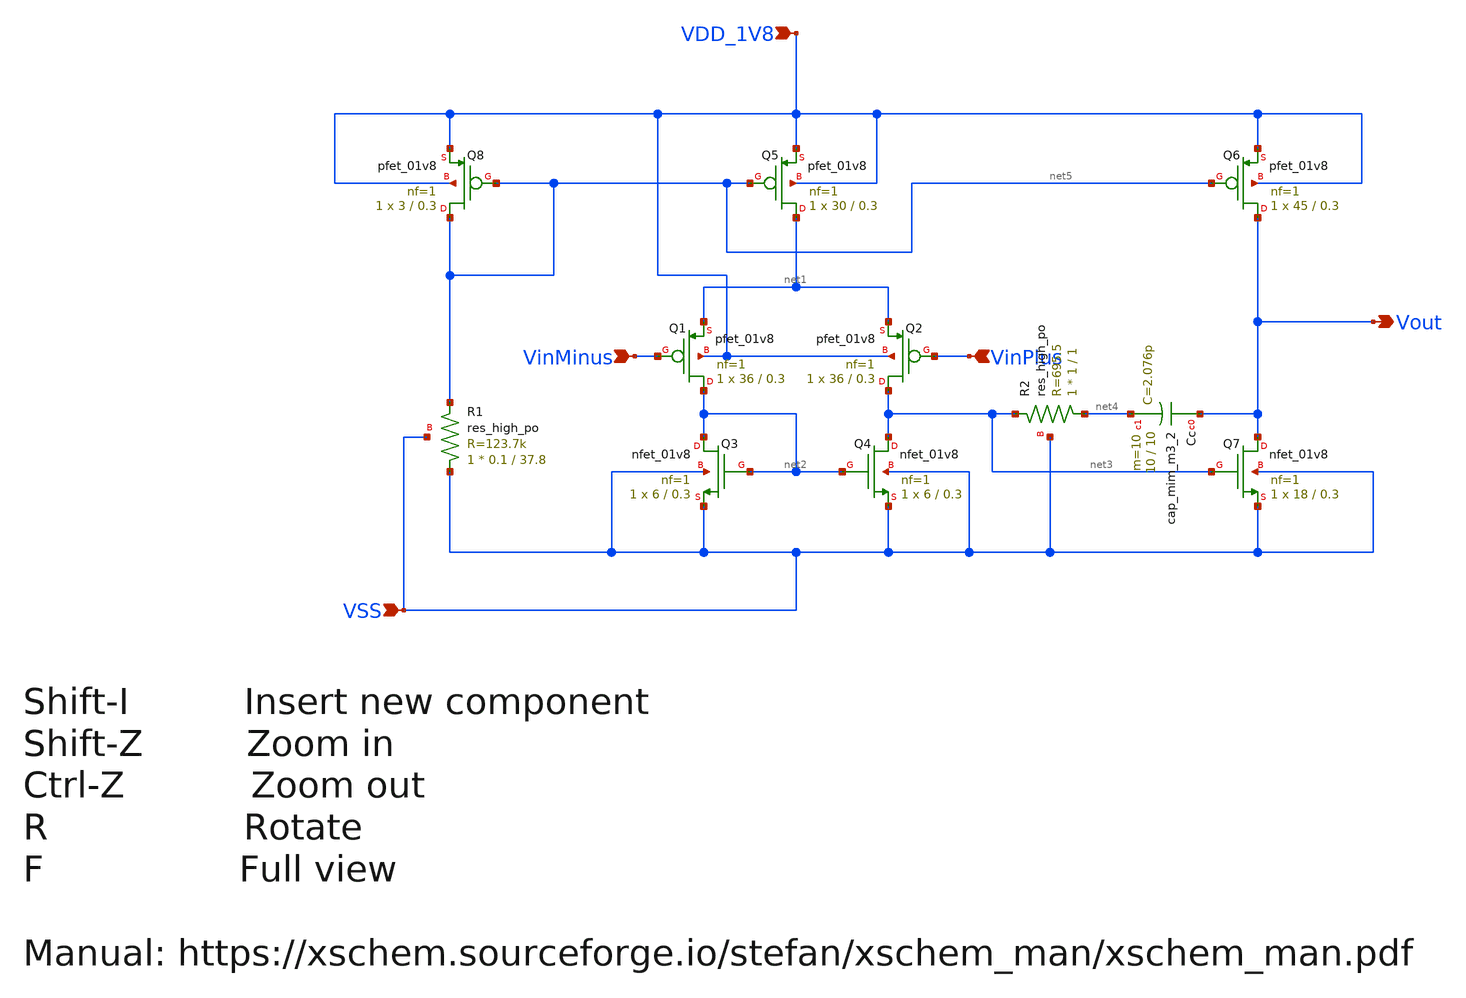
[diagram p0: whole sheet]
** sch_path: rply_mainopamp_sky130nm/design/RPLY_MAINOPAMP_SKY130NM/RPLY_MAINOPAMP.sch
**.subckt RPLY_MAINOPAMP Vout VinMinus VinPlus VDD_1V8 VSS
*.opin Vout
*.ipin VinMinus
*.ipin VinPlus
*.ipin VDD_1V8
*.ipin VSS
XQ8 net5 net5 VDD_1V8 VDD_1V8 sky130_fd_pr__pfet_01v8 L=0.3 W=3 nf=1 ad='int((nf+1)/2) * W/nf * 0.29'
+ as='int((nf+2)/2) * W/nf * 0.29' pd='2*int((nf+1)/2) * (W/nf + 0.29)' ps='2*int((nf+2)/2) * (W/nf + 0.29)'
+ nrd='0.29 / W' nrs='0.29 / W' sa=0 sb=0 sd=0 mult=1 m=1
XQ5 net1 net5 VDD_1V8 VDD_1V8 sky130_fd_pr__pfet_01v8 L=0.3 W=30 nf=1 ad='int((nf+1)/2) * W/nf * 0.29'
+ as='int((nf+2)/2) * W/nf * 0.29' pd='2*int((nf+1)/2) * (W/nf + 0.29)' ps='2*int((nf+2)/2) * (W/nf + 0.29)'
+ nrd='0.29 / W' nrs='0.29 / W' sa=0 sb=0 sd=0 mult=1 m=1
XQ6 Vout net5 VDD_1V8 VDD_1V8 sky130_fd_pr__pfet_01v8 L=0.3 W=45 nf=1 ad='int((nf+1)/2) * W/nf * 0.29'
+ as='int((nf+2)/2) * W/nf * 0.29' pd='2*int((nf+1)/2) * (W/nf + 0.29)' ps='2*int((nf+2)/2) * (W/nf + 0.29)'
+ nrd='0.29 / W' nrs='0.29 / W' sa=0 sb=0 sd=0 mult=1 m=1
XQ1 net2 VinMinus net1 VDD_1V8 sky130_fd_pr__pfet_01v8 L=0.3 W=36 nf=1 ad='int((nf+1)/2) * W/nf * 0.29'
+ as='int((nf+2)/2) * W/nf * 0.29' pd='2*int((nf+1)/2) * (W/nf + 0.29)' ps='2*int((nf+2)/2) * (W/nf + 0.29)'
+ nrd='0.29 / W' nrs='0.29 / W' sa=0 sb=0 sd=0 mult=1 m=1
XQ2 net3 VinPlus net1 VDD_1V8 sky130_fd_pr__pfet_01v8 L=0.3 W=36 nf=1 ad='int((nf+1)/2) * W/nf * 0.29'
+ as='int((nf+2)/2) * W/nf * 0.29' pd='2*int((nf+1)/2) * (W/nf + 0.29)' ps='2*int((nf+2)/2) * (W/nf + 0.29)'
+ nrd='0.29 / W' nrs='0.29 / W' sa=0 sb=0 sd=0 mult=1 m=1
XQ4 net3 net2 VSS VSS sky130_fd_pr__nfet_01v8 L=0.3 W=6 nf=1 ad='int((nf+1)/2) * W/nf * 0.29' as='int((nf+2)/2) * W/nf * 0.29'
+ pd='2*int((nf+1)/2) * (W/nf + 0.29)' ps='2*int((nf+2)/2) * (W/nf + 0.29)' nrd='0.29 / W' nrs='0.29 / W'
+ sa=0 sb=0 sd=0 mult=1 m=1
XQ3 net2 net2 VSS VSS sky130_fd_pr__nfet_01v8 L=0.3 W=6 nf=1 ad='int((nf+1)/2) * W/nf * 0.29' as='int((nf+2)/2) * W/nf * 0.29'
+ pd='2*int((nf+1)/2) * (W/nf + 0.29)' ps='2*int((nf+2)/2) * (W/nf + 0.29)' nrd='0.29 / W' nrs='0.29 / W'
+ sa=0 sb=0 sd=0 mult=1 m=1
XQ7 Vout net3 VSS VSS sky130_fd_pr__nfet_01v8 L=0.3 W=18 nf=1 ad='int((nf+1)/2) * W/nf * 0.29' as='int((nf+2)/2) * W/nf * 0.29'
+ pd='2*int((nf+1)/2) * (W/nf + 0.29)' ps='2*int((nf+2)/2) * (W/nf + 0.29)' nrd='0.29 / W' nrs='0.29 / W'
+ sa=0 sb=0 sd=0 mult=1 m=1
XCc Vout net4 sky130_fd_pr__cap_mim_m3_2 W=10 L=10 MF=10 m=10
XR1 VSS net5 VSS sky130_fd_pr__res_high_po W=0.1 L=37.8 mult=1 m=1
XR2 net4 net3 VSS sky130_fd_pr__res_high_po W=1 L=1 mult=1 m=1
**.ends
.end
